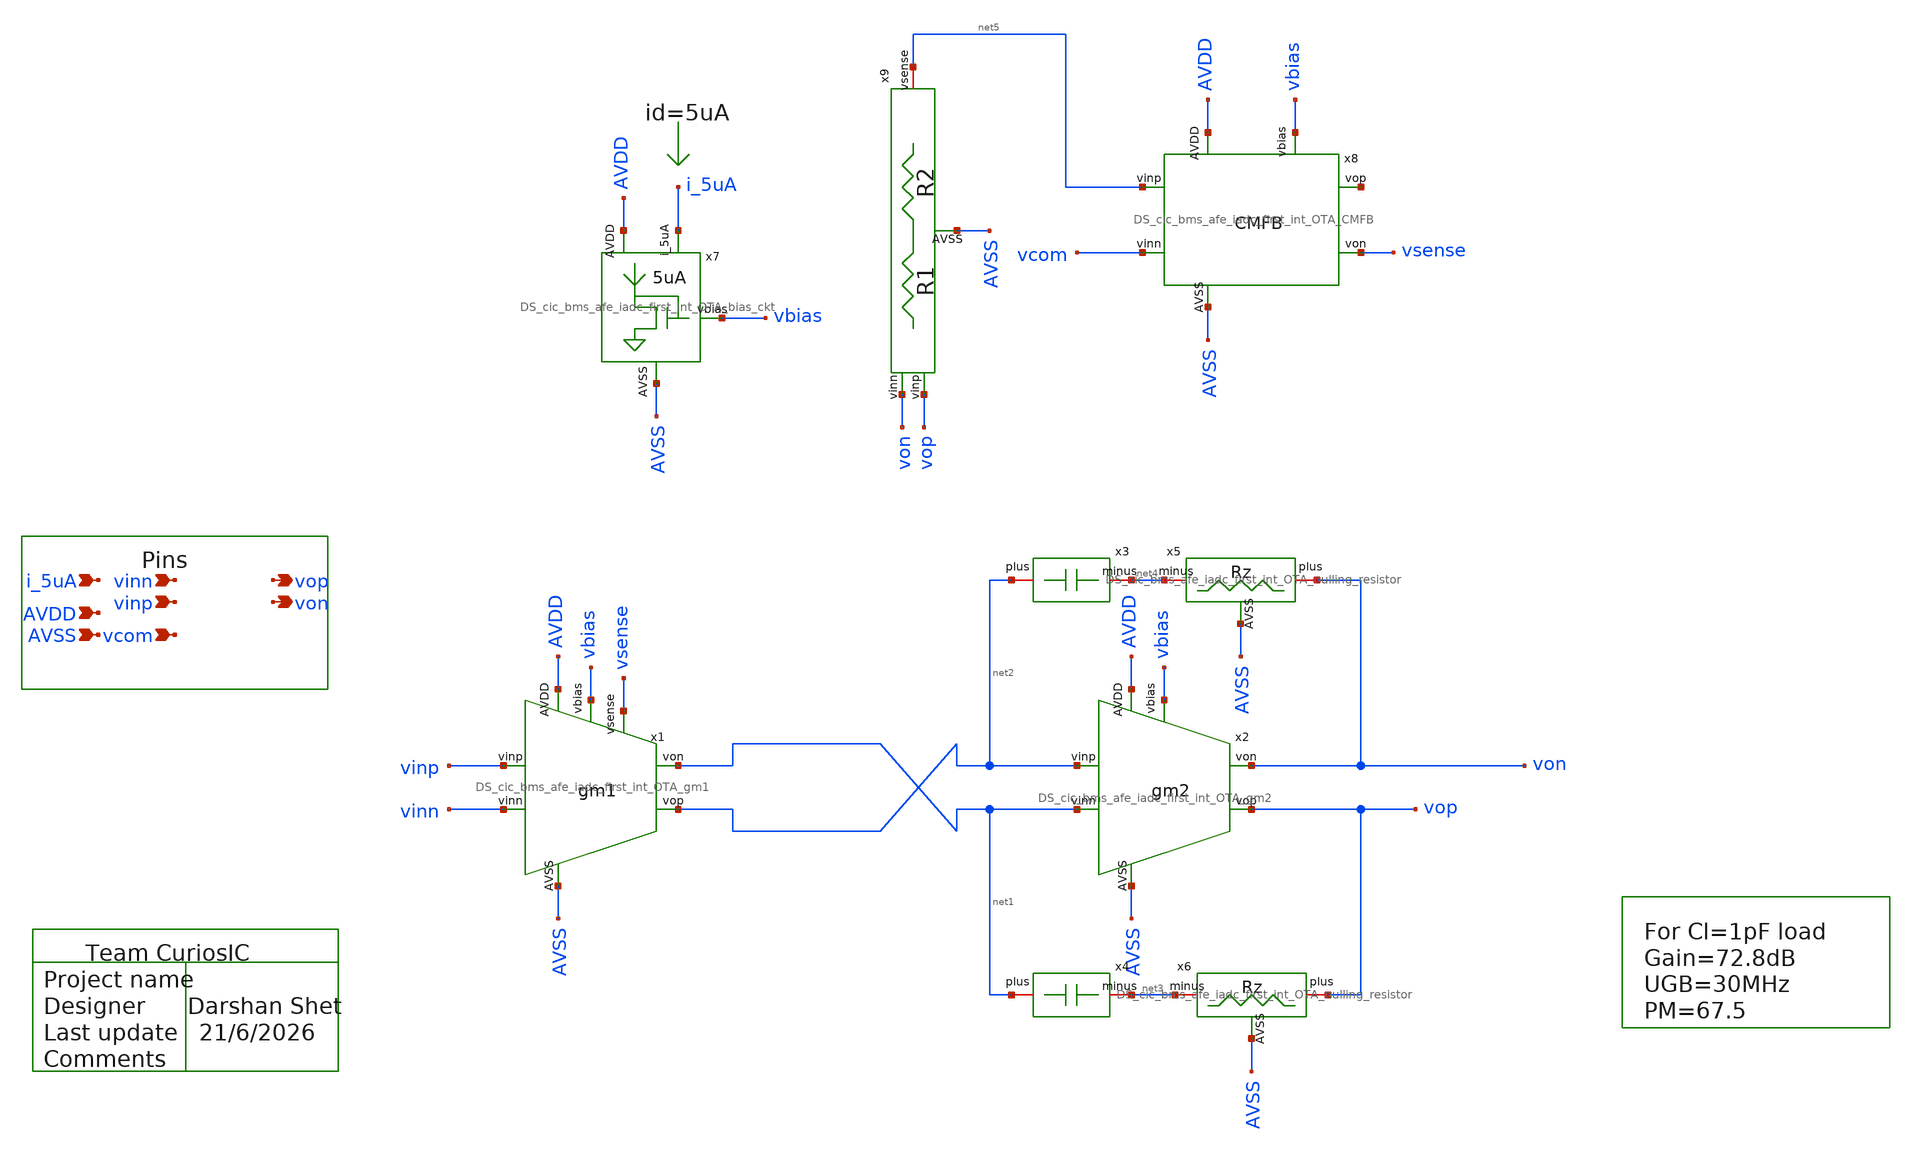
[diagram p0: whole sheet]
** sch_path: design/schematics/ADC/DSM_Loop_filter/First_int/OTA_Files/DS_cic_bms_afe_iadc_first_int_OTA.sch
**.subckt DS_cic_bms_afe_iadc_first_int_OTA i_5uA AVDD AVSS vinn vinp vcom vop von
*.ipin i_5uA
*.ipin AVDD
*.ipin AVSS
*.ipin vinn
*.ipin vinp
*.ipin vcom
*.opin vop
*.opin von
x1 net2 AVDD vinp vinn AVSS net1 vsense vbias DS_cic_bms_afe_iadc_first_int_OTA_gm1
x2 net2 AVDD vop net1 AVSS von vbias DS_cic_bms_afe_iadc_first_int_OTA_gm2
x3 net2 net4 DS_cic_bms_afe_iadc_first_int_OTA_miller_cap
x4 net1 net3 DS_cic_bms_afe_iadc_first_int_OTA_miller_cap
x5 von net4 AVSS DS_cic_bms_afe_iadc_first_int_OTA_nulling_resistor
x6 vop net3 AVSS DS_cic_bms_afe_iadc_first_int_OTA_nulling_resistor
x7 i_5uA AVSS AVDD vbias DS_cic_bms_afe_iadc_first_int_OTA_bias_ckt
x8 AVDD AVSS vcom net5 vbias net6 vsense DS_cic_bms_afe_iadc_first_int_OTA_CMFB
x9 von net5 vop AVSS DS_cic_bms_afe_iadc_first_int_OTA_CMFB_resistor_divider
**.ends
.end
